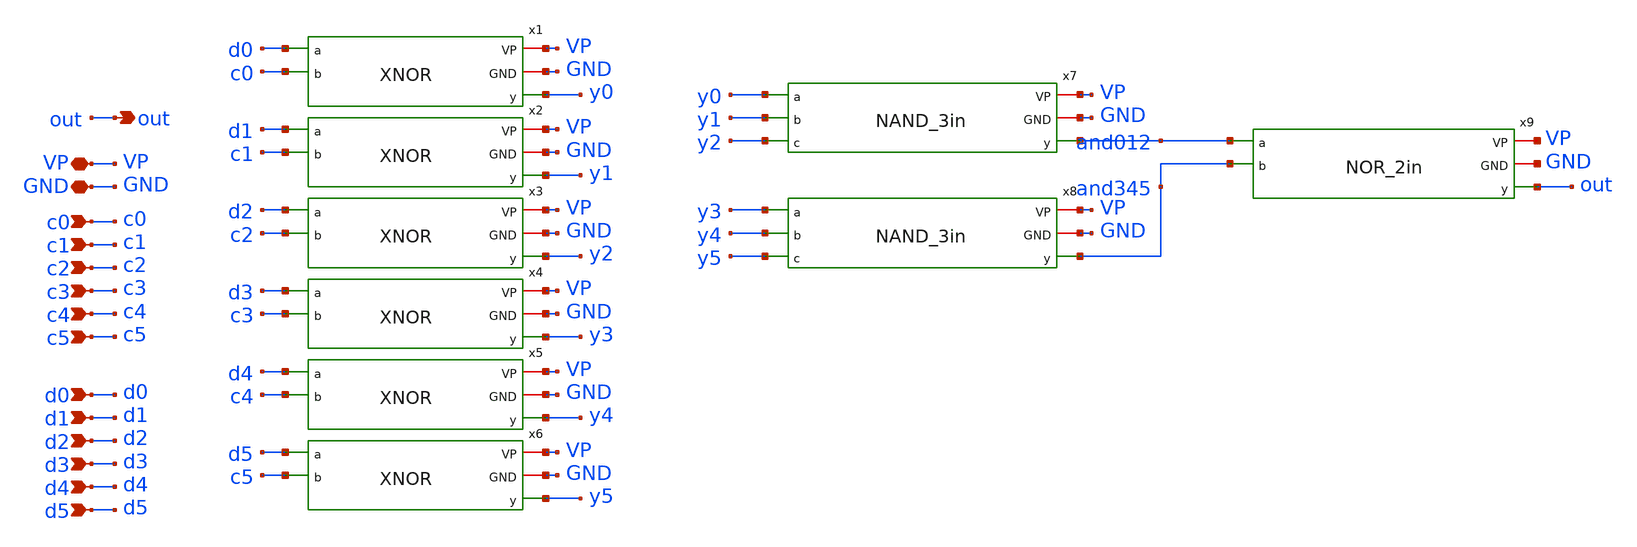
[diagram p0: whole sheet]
** sch_path: PLL0663-main/schematic/xschem/divider/count_data_check.sch
**.subckt count_data_check GND c0 VP c1 out c2 c3 c4 c5 d0 d1 d3 d4 d5 d2
*.iopin GND
*.ipin c0
*.iopin VP
*.ipin c1
*.opin out
*.ipin c2
*.ipin c3
*.ipin c4
*.ipin c5
*.ipin d0
*.ipin d1
*.ipin d3
*.ipin d4
*.ipin d5
*.ipin d2
x7 VP GND y0 and012 y1 y2 NAND_3in
x8 VP GND y3 and345 y4 y5 NAND_3in
x9 VP GND and012 out and345 NOR_2in
x1 VP GND d0 y0 c0 XNOR
x2 VP GND d1 y1 c1 XNOR
x3 VP GND d2 y2 c2 XNOR
x4 VP GND d3 y3 c3 XNOR
x5 VP GND d4 y4 c4 XNOR
x6 VP GND d5 y5 c5 XNOR
**.ends
.end
